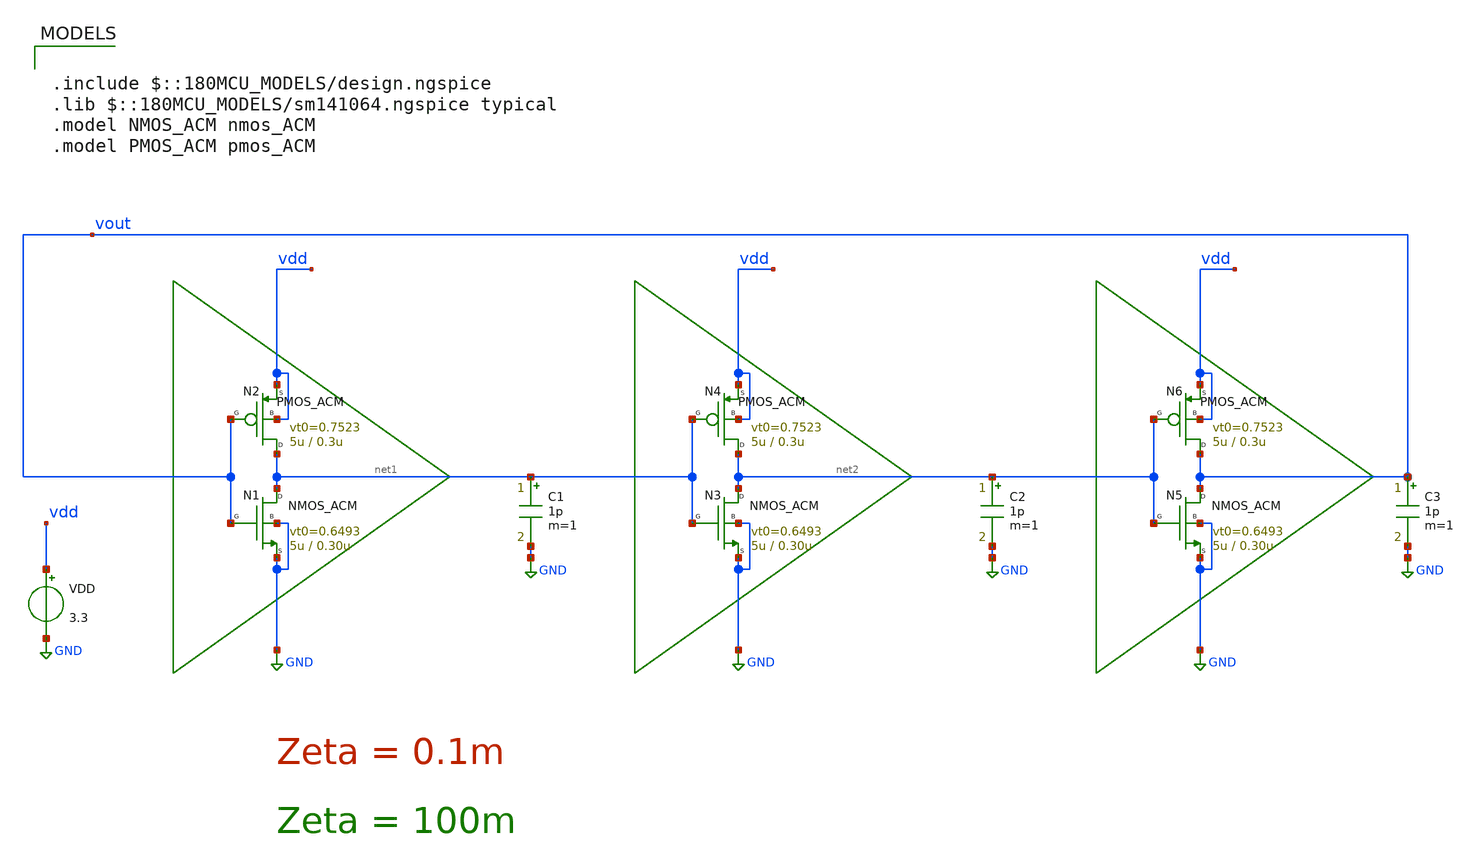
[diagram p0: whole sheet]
** sch_path: gf_tutorials/ACM/TB_rosc_acm.sch
**.subckt TB_rosc_acm
VDD vdd GND 3.3
C1 net1 GND 1p m=1
C2 net2 GND 1p m=1
C3 vout GND 1p m=1
N1 net1 vout GND GND NMOS_ACM w=5u l=0.30u n=1.383 is=1.076u vt0=0.6493 sigma=26.3m zeta={zeta_var}
N2 net1 vout vdd vdd PMOS_ACM w=5u l=0.3u n=1.42 is=0.35u vt0=0.7523 sigma=19.2m zeta={zeta_var}
N3 net2 net1 GND GND NMOS_ACM w=5u l=0.30u n=1.383 is=1.076u vt0=0.6493 sigma=26.3m zeta={zeta_var}
N4 net2 net1 vdd vdd PMOS_ACM w=5u l=0.3u n=1.42 is=0.35u vt0=0.7523 sigma=19.2m zeta={zeta_var}
N5 vout net2 GND GND NMOS_ACM w=5u l=0.30u n=1.383 is=1.076u vt0=0.6493 sigma=26.3m zeta={zeta_var}
N6 vout net2 vdd vdd PMOS_ACM w=5u l=0.3u n=1.42 is=0.35u vt0=0.7523 sigma=19.2m zeta={zeta_var}
**** begin user architecture code

.include $::180MCU_MODELS/design.ngspice
.lib $::180MCU_MODELS/sm141064.ngspice typical
.model NMOS_ACM nmos_ACM
.model PMOS_ACM pmos_ACM




.param zeta_var = 0.1m
.tran 1p 60n

.ic V(vout)=1.65
.control
pre_osdi /home/lci-ufsc/Desktop/work_gf180/ACM/NMOS_ACM_2V0.osdi
pre_osdi /home/lci-ufsc/Desktop/work_gf180/ACM/PMOS_ACM_2V0.osdi
save all

run
remzerovec
write TB_rosc_acm.raw
set appendwrite


alterparam zeta_var = 0.1
reset
run
remzerovec
write TB_rosc_acm.raw

.endc
.save all


**** end user architecture code
**.ends
.GLOBAL GND
.end
